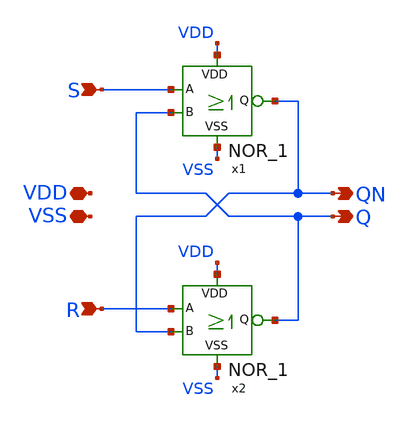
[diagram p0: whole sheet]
** sch_path: xschem/NOR-Latch/NOR_Latch.sch
* xschem/NOR/NOR_1.sch:
* Copyright 2022 Manuel Moser
* Licensed under the Apache License, Version 2.0 (the "License");
**.subckt NOR_Latch VDD VSS S R Q QN
*.iopin VDD
*.iopin VSS
*.ipin S
*.ipin R
*.opin Q
*.opin QN
x2 QN R VDD Q VSS NOR_1
x1 Q S VDD QN VSS NOR_1
**.ends

* expanding   symbol:  /foss/designs/SKY130_SAR-ADC/xschem/NOR/NOR_1.sym # of pins=5
** sym_path: xschem/NOR/NOR_1.sym
** sch_path: xschem/NOR/NOR_1.sch
.subckt NOR_1 B A VDD Q VSS
*.iopin VDD
*.iopin VSS
*.ipin B
*.ipin A
*.opin Q
XM5 Q B VSS VSS sky130_fd_pr__nfet_01v8 L=0.15 W=0.42 nf=1 ad='int((nf+1)/2) * W/nf * 0.29' as='int((nf+2)/2) * W/nf * 0.29'
+ pd='2*int((nf+1)/2) * (W/nf + 0.29)' ps='2*int((nf+2)/2) * (W/nf + 0.29)' nrd='0.29 / W' nrs='0.29 / W'
+ sa=0 sb=0 sd=0 mult=1 m=1
XM6 Q A VSS VSS sky130_fd_pr__nfet_01v8 L=0.15 W=0.42 nf=1 ad='int((nf+1)/2) * W/nf * 0.29' as='int((nf+2)/2) * W/nf * 0.29'
+ pd='2*int((nf+1)/2) * (W/nf + 0.29)' ps='2*int((nf+2)/2) * (W/nf + 0.29)' nrd='0.29 / W' nrs='0.29 / W'
+ sa=0 sb=0 sd=0 mult=1 m=1
XM1 Q B net1 VDD sky130_fd_pr__pfet_01v8 L=0.15 W=0.8 nf=1 ad='int((nf+1)/2) * W/nf * 0.29' as='int((nf+2)/2) * W/nf * 0.29'
+ pd='2*int((nf+1)/2) * (W/nf + 0.29)' ps='2*int((nf+2)/2) * (W/nf + 0.29)' nrd='0.29 / W' nrs='0.29 / W'
+ sa=0 sb=0 sd=0 mult=1 m=1
XM2 Q A net2 VDD sky130_fd_pr__pfet_01v8 L=0.15 W=0.8 nf=1 ad='int((nf+1)/2) * W/nf * 0.29' as='int((nf+2)/2) * W/nf * 0.29'
+ pd='2*int((nf+1)/2) * (W/nf + 0.29)' ps='2*int((nf+2)/2) * (W/nf + 0.29)' nrd='0.29 / W' nrs='0.29 / W'
+ sa=0 sb=0 sd=0 mult=1 m=1
XM3 net2 B VDD VDD sky130_fd_pr__pfet_01v8 L=0.15 W=0.8 nf=1 ad='int((nf+1)/2) * W/nf * 0.29' as='int((nf+2)/2) * W/nf * 0.29'
+ pd='2*int((nf+1)/2) * (W/nf + 0.29)' ps='2*int((nf+2)/2) * (W/nf + 0.29)' nrd='0.29 / W' nrs='0.29 / W'
+ sa=0 sb=0 sd=0 mult=1 m=1
XM4 net1 A VDD VDD sky130_fd_pr__pfet_01v8 L=0.15 W=0.8 nf=1 ad='int((nf+1)/2) * W/nf * 0.29' as='int((nf+2)/2) * W/nf * 0.29'
+ pd='2*int((nf+1)/2) * (W/nf + 0.29)' ps='2*int((nf+2)/2) * (W/nf + 0.29)' nrd='0.29 / W' nrs='0.29 / W'
+ sa=0 sb=0 sd=0 mult=1 m=1
.ends

.end
